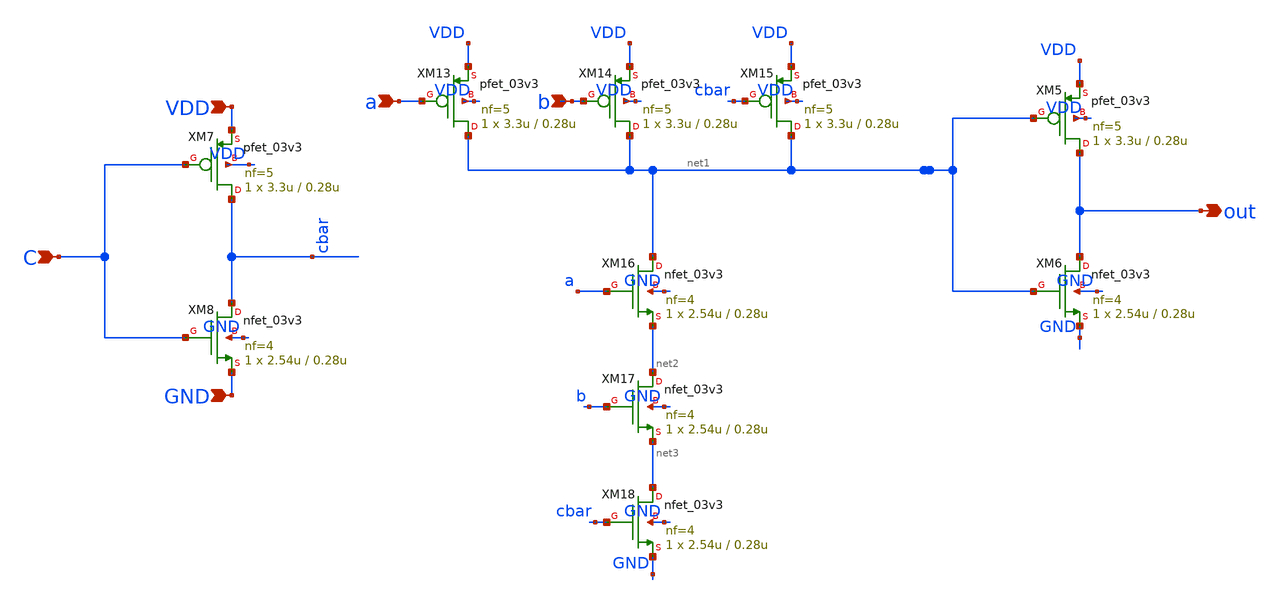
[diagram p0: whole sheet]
** sch_path: blocks/adc/encoder/sym/NAND3.sch
**.subckt NAND3 a out C b VDD GND
*.ipin a
*.opin out
*.ipin C
*.ipin b
*.ipin VDD
*.ipin GND
XM5 out net1 VDD VDD pfet_03v3 L=0.28u W=3.3u nf=5 ad='int((nf+1)/2) * W/nf * 0.18u' as='int((nf+2)/2) * W/nf * 0.18u'
+ pd='2*int((nf+1)/2) * (W/nf + 0.18u)' ps='2*int((nf+2)/2) * (W/nf + 0.18u)' nrd='0.18u / W' nrs='0.18u / W'
+ sa=0 sb=0 sd=0 m=1
XM6 out net1 GND GND nfet_03v3 L=0.28u W=2.54u nf=4 ad='int((nf+1)/2) * W/nf * 0.18u' as='int((nf+2)/2) * W/nf * 0.18u'
+ pd='2*int((nf+1)/2) * (W/nf + 0.18u)' ps='2*int((nf+2)/2) * (W/nf + 0.18u)' nrd='0.18u / W' nrs='0.18u / W'
+ sa=0 sb=0 sd=0 m=1
XM7 cbar C VDD VDD pfet_03v3 L=0.28u W=3.3u nf=5 ad='int((nf+1)/2) * W/nf * 0.18u' as='int((nf+2)/2) * W/nf * 0.18u'
+ pd='2*int((nf+1)/2) * (W/nf + 0.18u)' ps='2*int((nf+2)/2) * (W/nf + 0.18u)' nrd='0.18u / W' nrs='0.18u / W'
+ sa=0 sb=0 sd=0 m=1
XM8 cbar C GND GND nfet_03v3 L=0.28u W=2.54u nf=4 ad='int((nf+1)/2) * W/nf * 0.18u' as='int((nf+2)/2) * W/nf * 0.18u'
+ pd='2*int((nf+1)/2) * (W/nf + 0.18u)' ps='2*int((nf+2)/2) * (W/nf + 0.18u)' nrd='0.18u / W' nrs='0.18u / W'
+ sa=0 sb=0 sd=0 m=1
XM13 net1 a VDD VDD pfet_03v3 L=0.28u W=3.3u nf=5 ad='int((nf+1)/2) * W/nf * 0.18u' as='int((nf+2)/2) * W/nf * 0.18u'
+ pd='2*int((nf+1)/2) * (W/nf + 0.18u)' ps='2*int((nf+2)/2) * (W/nf + 0.18u)' nrd='0.18u / W' nrs='0.18u / W'
+ sa=0 sb=0 sd=0 m=1
XM14 net1 b VDD VDD pfet_03v3 L=0.28u W=3.3u nf=5 ad='int((nf+1)/2) * W/nf * 0.18u' as='int((nf+2)/2) * W/nf * 0.18u'
+ pd='2*int((nf+1)/2) * (W/nf + 0.18u)' ps='2*int((nf+2)/2) * (W/nf + 0.18u)' nrd='0.18u / W' nrs='0.18u / W'
+ sa=0 sb=0 sd=0 m=1
XM15 net1 cbar VDD VDD pfet_03v3 L=0.28u W=3.3u nf=5 ad='int((nf+1)/2) * W/nf * 0.18u' as='int((nf+2)/2) * W/nf * 0.18u'
+ pd='2*int((nf+1)/2) * (W/nf + 0.18u)' ps='2*int((nf+2)/2) * (W/nf + 0.18u)' nrd='0.18u / W' nrs='0.18u / W'
+ sa=0 sb=0 sd=0 m=1
XM16 net1 a net2 GND nfet_03v3 L=0.28u W=2.54u nf=4 ad='int((nf+1)/2) * W/nf * 0.18u' as='int((nf+2)/2) * W/nf * 0.18u'
+ pd='2*int((nf+1)/2) * (W/nf + 0.18u)' ps='2*int((nf+2)/2) * (W/nf + 0.18u)' nrd='0.18u / W' nrs='0.18u / W'
+ sa=0 sb=0 sd=0 m=1
XM17 net2 b net3 GND nfet_03v3 L=0.28u W=2.54u nf=4 ad='int((nf+1)/2) * W/nf * 0.18u' as='int((nf+2)/2) * W/nf * 0.18u'
+ pd='2*int((nf+1)/2) * (W/nf + 0.18u)' ps='2*int((nf+2)/2) * (W/nf + 0.18u)' nrd='0.18u / W' nrs='0.18u / W'
+ sa=0 sb=0 sd=0 m=1
XM18 net3 cbar GND GND nfet_03v3 L=0.28u W=2.54u nf=4 ad='int((nf+1)/2) * W/nf * 0.18u' as='int((nf+2)/2) * W/nf * 0.18u'
+ pd='2*int((nf+1)/2) * (W/nf + 0.18u)' ps='2*int((nf+2)/2) * (W/nf + 0.18u)' nrd='0.18u / W' nrs='0.18u / W'
+ sa=0 sb=0 sd=0 m=1
**.ends
.end
